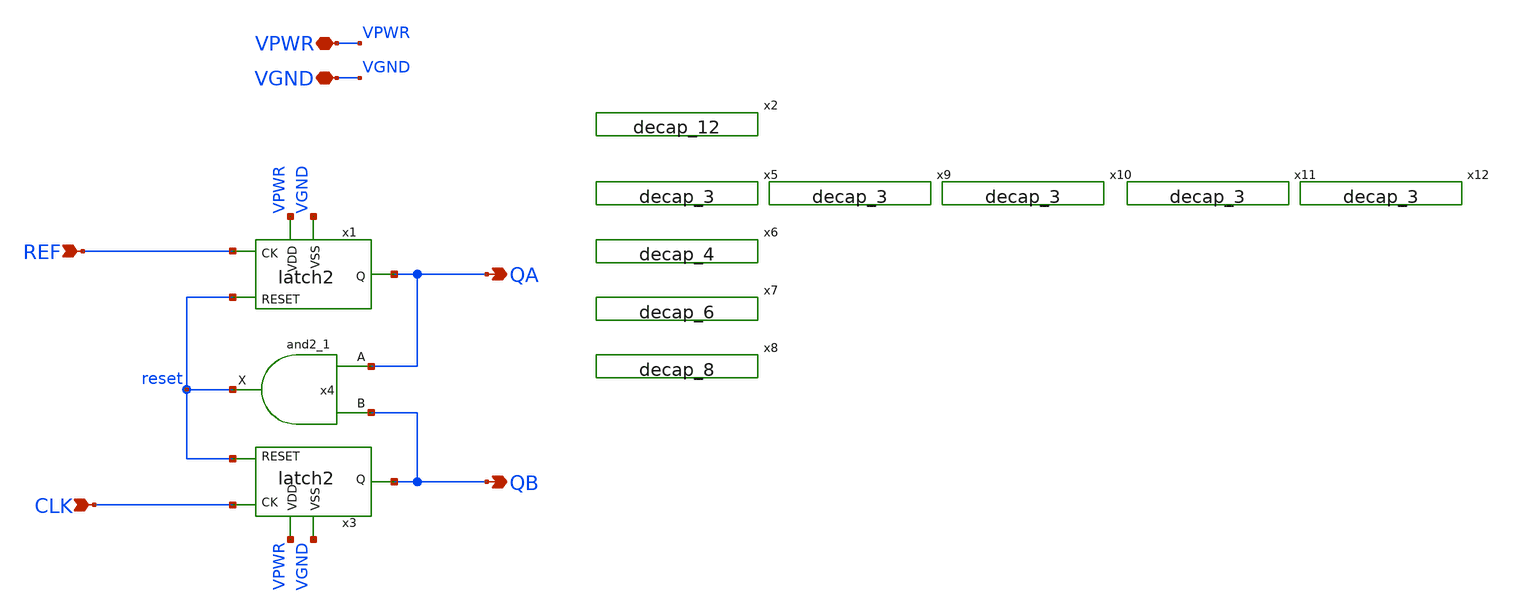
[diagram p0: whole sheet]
** sch_path: xschem/pfd.sch
**.subckt pfd VPWR REF VGND QA QB CLK
*.iopin VPWR
*.ipin REF
*.iopin VGND
*.opin QA
*.opin QB
*.ipin CLK
x1 REF QA reset VPWR VGND latch2
x3 CLK QB reset VPWR VGND latch2
x4 QA QB vgnd vgnd vpwr vpwr reset sky130_fd_sc_hd__and2_1
x2 vgnd vgnd vpwr vpwr sky130_fd_sc_hd__decap_12
x5 vgnd vgnd vpwr vpwr sky130_fd_sc_hd__decap_3
x6 vgnd vgnd vpwr vpwr sky130_fd_sc_hd__decap_4
x7 vgnd vgnd vpwr vpwr sky130_fd_sc_hd__decap_6
x8 vgnd vgnd vpwr vpwr sky130_fd_sc_hd__decap_8
x9 vgnd vgnd vpwr vpwr sky130_fd_sc_hd__decap_3
x10 vgnd vgnd vpwr vpwr sky130_fd_sc_hd__decap_3
x11 vgnd vgnd vpwr vpwr sky130_fd_sc_hd__decap_3
x12 vgnd vgnd vpwr vpwr sky130_fd_sc_hd__decap_3
**.ends

* expanding   symbol:  latch2.sym # of pins=5
** sym_path: xschem/latch2.sym
** sch_path: xschem/latch2.sch
.subckt latch2 CK Q RESET VDD VSS
*.ipin RESET
*.ipin CK
*.opin Q
*.ipin VDD
*.ipin VSS
x1 net3 net2 VSS VSS VDD VDD net1 sky130_fd_sc_hd__nor2_1
x2 net1 RESET VSS VSS VDD VDD net2 sky130_fd_sc_hd__nor2_1
x3 CK Q VSS VSS VDD VDD net3 sky130_fd_sc_hd__nor2_1
x4 net3 net1 VSS VSS VDD VDD Q sky130_fd_sc_hd__nor2_4
.ends

.end
